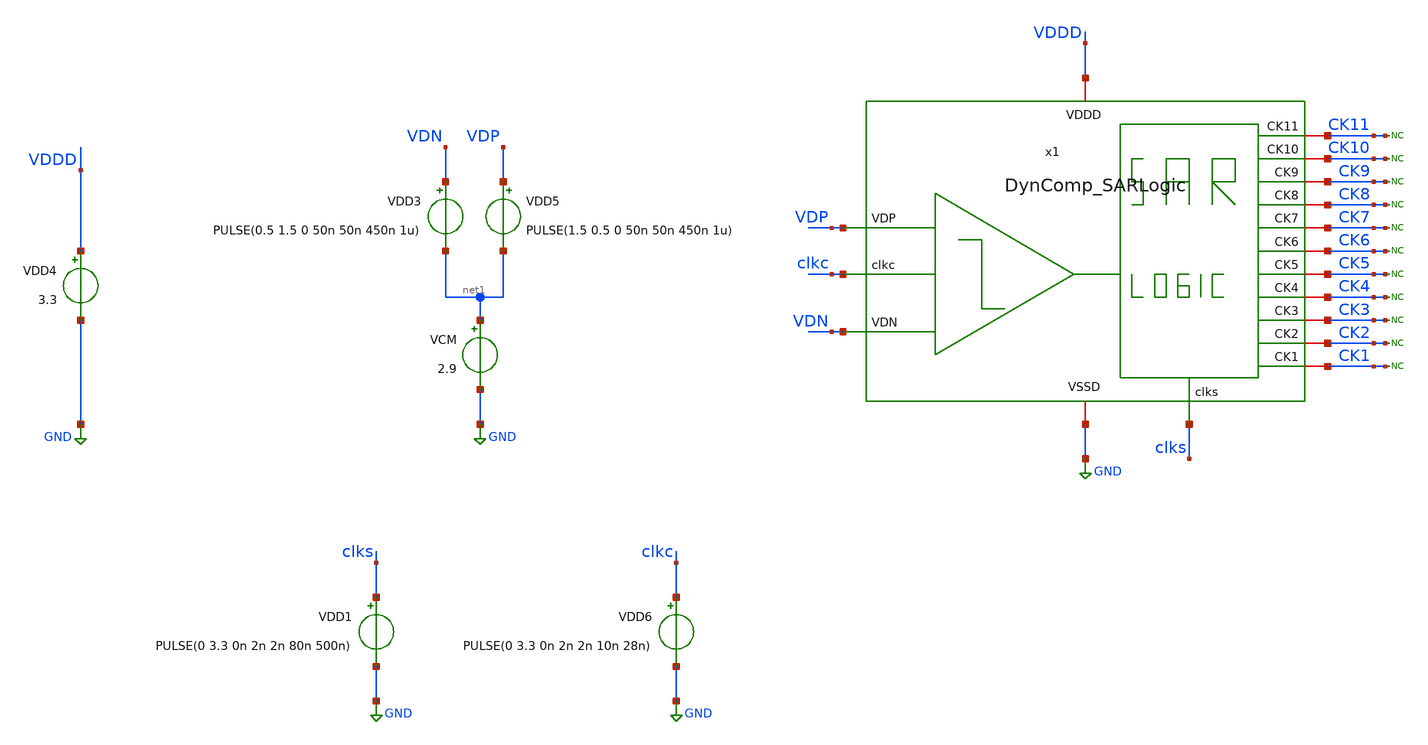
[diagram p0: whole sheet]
** sch_path: SAR_ADC/integration/DynComp_SARLogic_tb.sch
**.subckt DynComp_SARLogic_tb
x1 clks clkc CK11 VDDD CK10 GND CK9 CK8 CK7 VDP CK6 VDN CK5 CK4 CK3 CK2 CK1 DynComp_SARLogic
VDD4 VDDD GND 3.3
VDD3 VDN net1 PULSE(0.5 1.5 0 50n 50n 450n 1u)
VCM net1 GND 2.9
VDD5 VDP net1 PULSE(1.5 0.5 0 50n 50n 450n 1u)
* noconn CK11
* noconn CK10
* noconn CK9
* noconn CK8
* noconn CK7
* noconn CK6
* noconn CK5
* noconn CK4
* noconn CK3
* noconn CK2
* noconn CK1
VDD1 clks GND PULSE(0 3.3 0n 2n 2n 80n 500n)
VDD6 clkc GND PULSE(0 3.3 0n 2n 2n 10n 28n)
**** begin user architecture code



*Parameters

.options TEMP = 50.0
.lib /home/electrica/Documents/gf180_projects/pdk/gf180mcuC/libs.tech/ngspice/sm141064.ngspice typical
.include /home/electrica/Documents/gf180_projects/pdk/gf180mcuC/libs.tech/ngspice/design.ngspice

*Data to save
.save all

* Simulation
.control
tran 0.5n 4u
setplot dc1
plot V(clkc)+36 V(VDN)+32 V(VDP)+32 V(clkc)+28 V(.x1.x1.aN)+24 V(.x1.x1.aP)+20 V(.x1.x1.dN)+16
+ V(.x1.x1.dP)+12 V(.x1.x1.Vocn)+8 V(.x1.x1.Vocp)+4 V(.x1.Valid)
set filetype = ascii
write DynComp_SARLogic_tb_tran.raw

reset
unset filetype
op
save all
write DynComp_SARLogic_tb.raw


.endc
.end


**** end user architecture code
**.ends
.GLOBAL GND
.end
